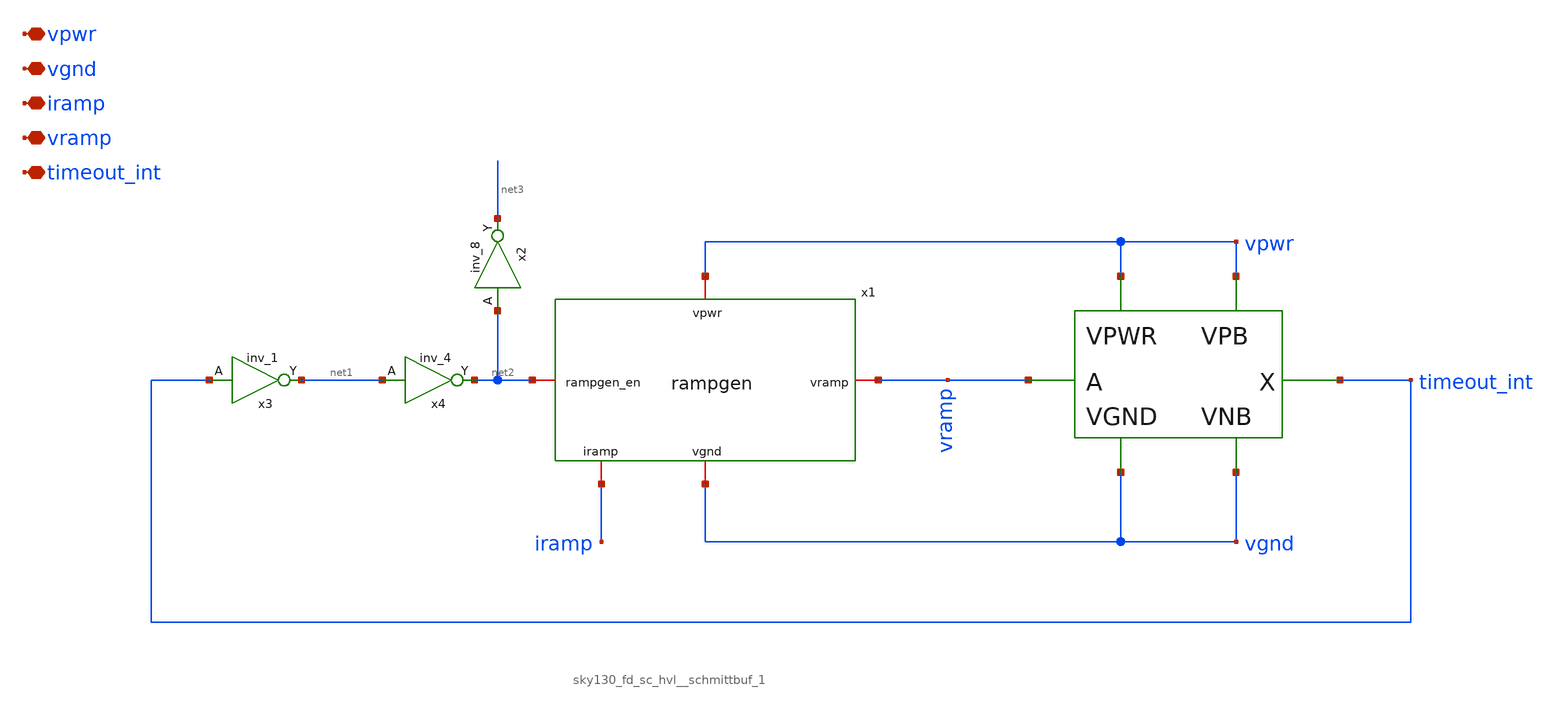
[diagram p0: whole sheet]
** sch_path: images/iic-osic-tools/addons/examples/open-pmic/design/oscillator/oscillator.sch
**.subckt oscillator vpwr vgnd iramp vramp timeout_int
*.iopin vpwr
*.iopin vgnd
*.iopin iramp
*.iopin vramp
*.iopin timeout_int
x1 vpwr vgnd iramp vramp net2 rampgen
x3 timeout_int vgnd vgnd vpwr vpwr net1 sky130_fd_sc_hvl__inv_1
x4 net1 vgnd vgnd vpwr vpwr net2 sky130_fd_sc_hvl__inv_4
x5 vramp vgnd vgnd vpwr vpwr timeout_int sky130_fd_sc_hvl__schmittbuf_1
x2 net2 vgnd vgnd vpwr vpwr net3 sky130_fd_sc_hvl__inv_8
**** begin user architecture code

.include $::SKYWATER_MODELS/cells/nfet_01v8/sky130_fd_pr__nfet_01v8__tt.corner.spice
.include $::SKYWATER_MODELS/cells/nfet_01v8_lvt/sky130_fd_pr__nfet_01v8_lvt__tt.corner.spice
.include $::SKYWATER_MODELS/cells/pfet_01v8/sky130_fd_pr__pfet_01v8__tt.corner.spice
.include $::SKYWATER_MODELS/cells/nfet_03v3_nvt/sky130_fd_pr__nfet_03v3_nvt__tt.corner.spice
.include $::SKYWATER_MODELS/cells/nfet_05v0_nvt/sky130_fd_pr__nfet_05v0_nvt__tt.corner.spice
.include $::SKYWATER_MODELS/cells/esd_nfet_01v8/sky130_fd_pr__esd_nfet_01v8__tt.corner.spice
.include $::SKYWATER_MODELS/cells/pfet_01v8_lvt/sky130_fd_pr__pfet_01v8_lvt__tt.corner.spice
.include $::SKYWATER_MODELS/cells/pfet_01v8_hvt/sky130_fd_pr__pfet_01v8_hvt__tt.corner.spice
.include $::SKYWATER_MODELS/cells/esd_pfet_g5v0d10v5/sky130_fd_pr__esd_pfet_g5v0d10v5__tt.corner.spice
.include $::SKYWATER_MODELS/cells/pfet_g5v0d10v5/sky130_fd_pr__pfet_g5v0d10v5__tt.corner.spice
.include $::SKYWATER_MODELS/cells/pfet_g5v0d16v0/sky130_fd_pr__pfet_g5v0d16v0__tt.corner.spice
.include $::SKYWATER_MODELS/cells/nfet_g5v0d10v5/sky130_fd_pr__nfet_g5v0d10v5__tt.corner.spice
.include $::SKYWATER_MODELS/cells/nfet_g5v0d16v0/sky130_fd_pr__nfet_g5v0d16v0__tt_discrete.corner.spice
.include $::SKYWATER_MODELS/cells/esd_nfet_g5v0d10v5/sky130_fd_pr__esd_nfet_g5v0d10v5__tt.corner.spice
.include $::SKYWATER_MODELS/models/corners/tt/nonfet.spice
* Mismatch parameters
.include $::SKYWATER_MODELS/cells/nfet_01v8/sky130_fd_pr__nfet_01v8__mismatch.corner.spice
.include $::SKYWATER_MODELS/cells/pfet_01v8/sky130_fd_pr__pfet_01v8__mismatch.corner.spice
.include $::SKYWATER_MODELS/cells/nfet_01v8_lvt/sky130_fd_pr__nfet_01v8_lvt__mismatch.corner.spice
.include $::SKYWATER_MODELS/cells/pfet_01v8_lvt/sky130_fd_pr__pfet_01v8_lvt__mismatch.corner.spice
.include $::SKYWATER_MODELS/cells/pfet_01v8_hvt/sky130_fd_pr__pfet_01v8_hvt__mismatch.corner.spice
.include $::SKYWATER_MODELS/cells/nfet_g5v0d10v5/sky130_fd_pr__nfet_g5v0d10v5__mismatch.corner.spice
.include $::SKYWATER_MODELS/cells/pfet_g5v0d10v5/sky130_fd_pr__pfet_g5v0d10v5__mismatch.corner.spice
.include $::SKYWATER_MODELS/cells/nfet_05v0_nvt/sky130_fd_pr__nfet_05v0_nvt__mismatch.corner.spice
.include $::SKYWATER_MODELS/cells/nfet_03v3_nvt/sky130_fd_pr__nfet_03v3_nvt__mismatch.corner.spice
* Resistor$::SKYWATER_MODELS/Capacitor
.include $::SKYWATER_MODELS/models/r+c/res_typical__cap_typical.spice
.include $::SKYWATER_MODELS/models/r+c/res_typical__cap_typical__lin.spice
* Special cells
.include $::SKYWATER_MODELS/models/corners/tt/specialized_cells.spice
* All models
.include $::SKYWATER_MODELS/models/all.spice
* Corner
.include $::SKYWATER_MODELS/models/corners/tt/rf.spice



.include /home/atumkur/EE272B/open-pmic/layout/oscillator/schmittbuf_lvs.spice
.include /usr/share/pdk/sky130A/libs.ref/sky130_fd_sc_hvl/spice/sky130_fd_sc_hvl.spice


**** end user architecture code
**.ends
**** begin user architecture code
[sky130_models]
**** end user architecture code
.end
